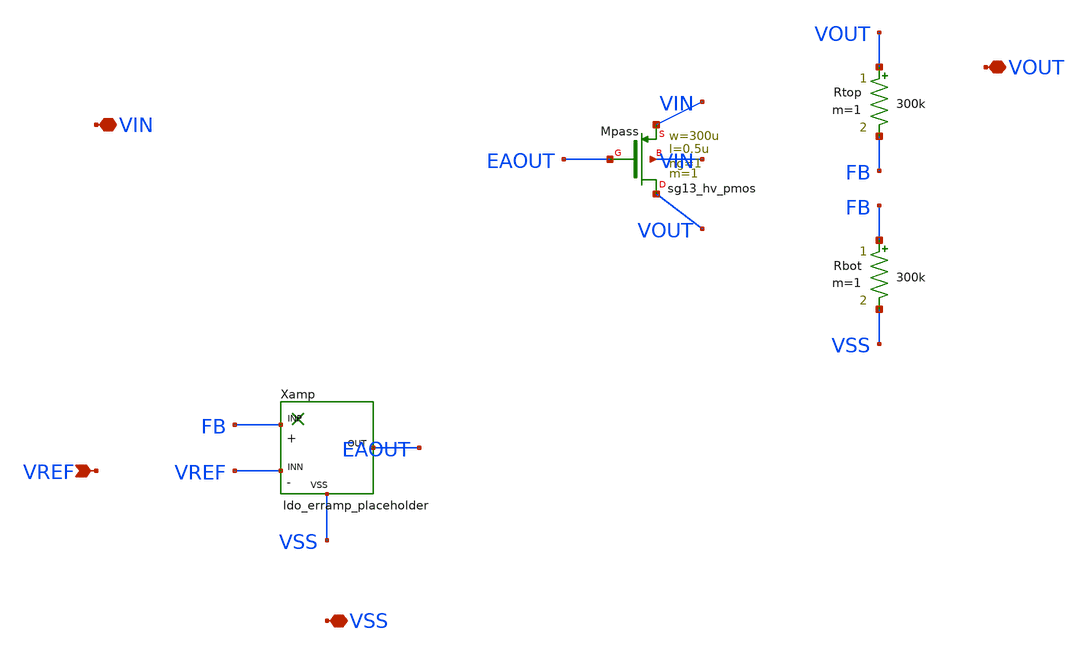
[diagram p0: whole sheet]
** sch_path: design/ldo_core.sch
**.subckt ldo_core VIN VOUT VSS VREF
*.iopin VIN
*.iopin VOUT
*.iopin VSS
*.ipin VREF
XMpass VOUT EAOUT VIN VIN sg13_hv_pmos w=300u l=0.5u ng=1 m=1 mm_ok=1
Rtop VOUT FB 300k m=1
Rbot FB VSS 300k m=1
Xamp FB VREF EAOUT VSS ldo_erramp_placeholder
**.ends

* expanding   symbol:  ldo_erramp_placeholder.sym # of pins=4
** sym_path: design/ldo_erramp_placeholder.sym
** sch_path: design/ldo_erramp_placeholder.sch
.subckt ldo_erramp_placeholder INP INN OUT VSS
*.ipin INP
*.ipin INN
*.opin OUT
*.iopin VSS
E1 OUT VSS INP INN 100k
.ends

.end
